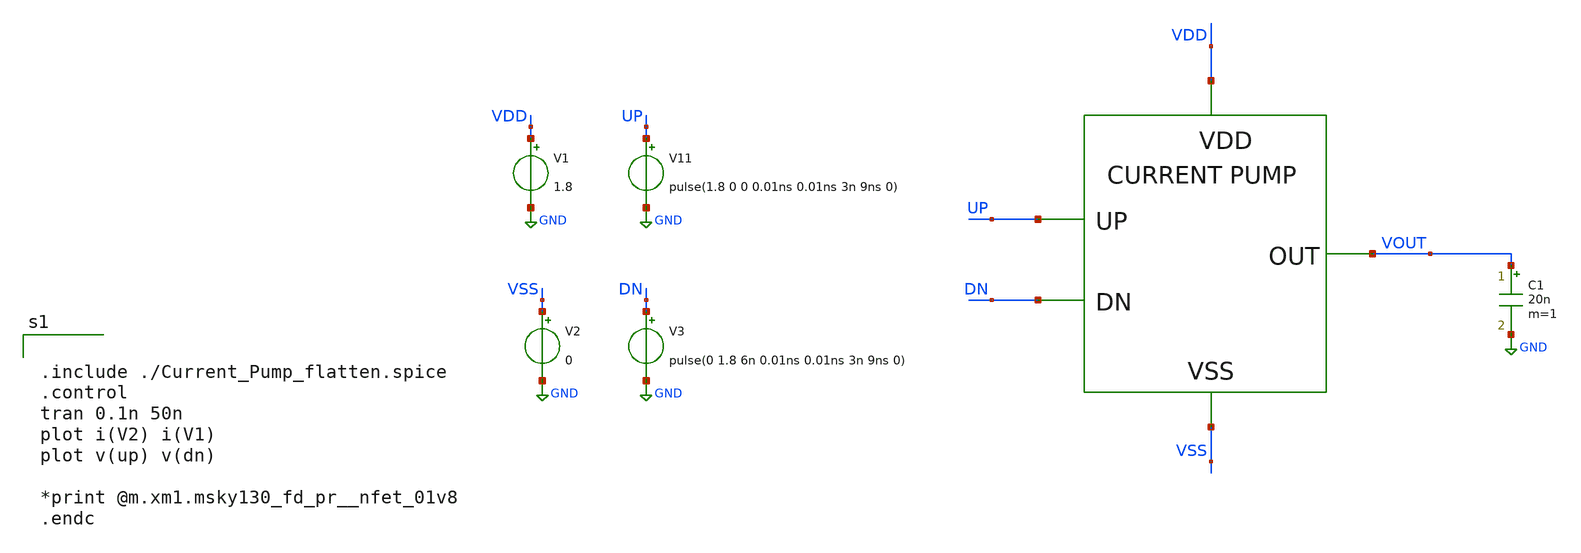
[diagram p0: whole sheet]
** sch_path: xschem/DC_DC_Converter_xschem/DC_DC_Converter/current_pump/current_pump_PEX_TB.sch
**.subckt current_pump_PEX_TB
C1 VOUT GND 20n m=1
V11 UP GND pulse(1.8 0 0 0.01ns 0.01ns 3n 9ns 0)
V3 DN GND pulse(0 1.8 6n 0.01ns 0.01ns 3n 9ns 0)
V1 VDD GND 1.8
V2 VSS GND 0
X1 UP VOUT VDD VSS DN current_pump_PEX
**** begin user architecture code

** opencircuitdesign pdks install
.lib $::SKYWATER_MODELS/sky130.lib.spice tt




.include ./Current_Pump_flatten.spice
.control
tran 0.1n 50n
plot i(V2) i(V1)
plot v(up) v(dn)

*print @m.xm1.msky130_fd_pr__nfet_01v8
.endc


**** end user architecture code
**.ends
.GLOBAL GND
.end
